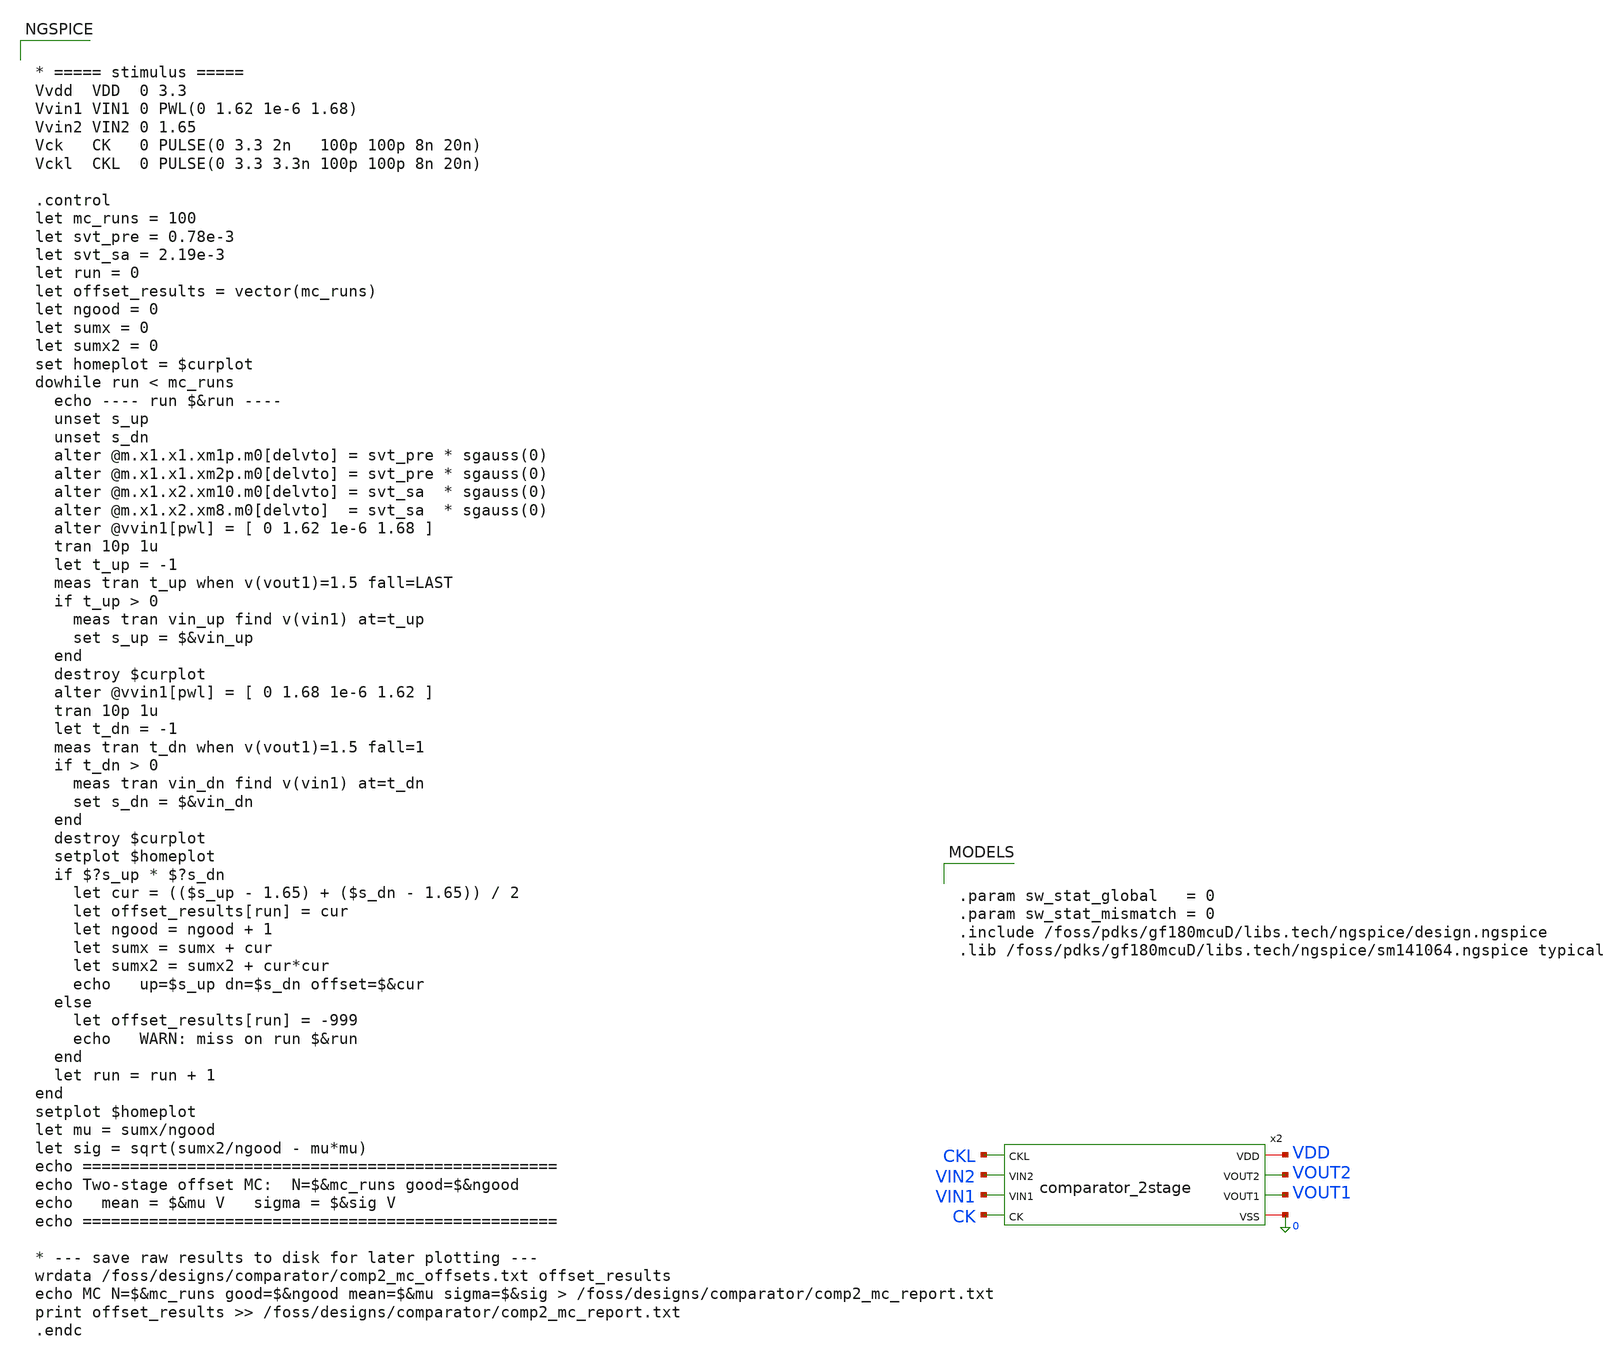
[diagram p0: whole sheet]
** sch_path: comparator_alt/schematic/tb_2stage.sch
**.subckt tb_2stage
x2 CKL VIN2 VDD VOUT2 VIN1 VOUT1 CK 0 comparator_2stage
**** begin user architecture code


.param sw_stat_global   = 0
.param sw_stat_mismatch = 0
.include /foss/pdks/gf180mcuD/libs.tech/ngspice/design.ngspice
.lib /foss/pdks/gf180mcuD/libs.tech/ngspice/sm141064.ngspice typical




* ===== stimulus =====
Vvdd  VDD  0 3.3
Vvin1 VIN1 0 PWL(0 1.62 1e-6 1.68)
Vvin2 VIN2 0 1.65
Vck   CK   0 PULSE(0 3.3 2n   100p 100p 8n 20n)
Vckl  CKL  0 PULSE(0 3.3 3.3n 100p 100p 8n 20n)

.control
let mc_runs = 100
let svt_pre = 0.78e-3
let svt_sa = 2.19e-3
let run = 0
let offset_results = vector(mc_runs)
let ngood = 0
let sumx = 0
let sumx2 = 0
set homeplot = $curplot
dowhile run < mc_runs
  echo ---- run $&run ----
  unset s_up
  unset s_dn
  alter @m.x1.x1.xm1p.m0[delvto] = svt_pre * sgauss(0)
  alter @m.x1.x1.xm2p.m0[delvto] = svt_pre * sgauss(0)
  alter @m.x1.x2.xm10.m0[delvto] = svt_sa  * sgauss(0)
  alter @m.x1.x2.xm8.m0[delvto]  = svt_sa  * sgauss(0)
  alter @vvin1[pwl] = [ 0 1.62 1e-6 1.68 ]
  tran 10p 1u
  let t_up = -1
  meas tran t_up when v(vout1)=1.5 fall=LAST
  if t_up > 0
    meas tran vin_up find v(vin1) at=t_up
    set s_up = $&vin_up
  end
  destroy $curplot
  alter @vvin1[pwl] = [ 0 1.68 1e-6 1.62 ]
  tran 10p 1u
  let t_dn = -1
  meas tran t_dn when v(vout1)=1.5 fall=1
  if t_dn > 0
    meas tran vin_dn find v(vin1) at=t_dn
    set s_dn = $&vin_dn
  end
  destroy $curplot
  setplot $homeplot
  if $?s_up * $?s_dn
    let cur = (($s_up - 1.65) + ($s_dn - 1.65)) / 2
    let offset_results[run] = cur
    let ngood = ngood + 1
    let sumx = sumx + cur
    let sumx2 = sumx2 + cur*cur
    echo   up=$s_up dn=$s_dn offset=$&cur
  else
    let offset_results[run] = -999
    echo   WARN: miss on run $&run
  end
  let run = run + 1
end
setplot $homeplot
let mu = sumx/ngood
let sig = sqrt(sumx2/ngood - mu*mu)
echo ==================================================
echo Two-stage offset MC:  N=$&mc_runs good=$&ngood
echo   mean = $&mu V   sigma = $&sig V
echo ==================================================

* --- save raw results to disk for later plotting ---
wrdata /foss/designs/comparator/comp2_mc_offsets.txt offset_results
echo MC N=$&mc_runs good=$&ngood mean=$&mu sigma=$&sig >
+ /foss/designs/comparator/comp2_mc_report.txt
print offset_results >> /foss/designs/comparator/comp2_mc_report.txt
.endc


**** end user architecture code
**.ends

* expanding   symbol:  comparator_alt/schematic/comparator_2stage.sym # of pins=8
** sym_path: comparator/schematic/comparator_2stage.sym
** sch_path: comparator/schematic/comparator_2stage.sch
.subckt comparator_2stage CKL VIN2 VDD VOUT2 VIN1 VOUT1 CK VSS
*.ipin CK
*.iopin VDD
*.iopin VSS
*.ipin VIN1
*.ipin VIN2
*.opin VOUT2
*.opin VOUT1
*.ipin CKL
x2 VDD DIP1 DIP2 VIN2 VIN1 CK VSS preamp_dyn
x4 VDD CKL VOUT2 VOUT1 DIP2 DIP1 VSS strongarm_2
.ends


* expanding   symbol:  comparator/schematic/preamp_dyn.sym # of pins=7
** sym_path: comparator_alt/schematic/preamp_dyn.sym
** sch_path: comparator_alt/schematic/preamp_dyn.sch
.subckt preamp_dyn VDD DIP2 DIP1 VIN2 VIN1 CK VSS
*.ipin VIN1
*.ipin VIN2
*.iopin VDD
*.iopin VSS
*.opin DIP1
*.opin DIP2
*.ipin CK
XM1P DIP1 VIN1 TAIL VSS nfet_03v3 L=1u W=4u nf=1 ad='int((nf+1)/2) * W/nf * 0.18u' as='int((nf+2)/2) * W/nf * 0.18u'
+ pd='2*int((nf+1)/2) * (W/nf + 0.18u)' ps='2*int((nf+2)/2) * (W/nf + 0.18u)' nrd='0.18u / W' nrs='0.18u / W'
+ sa=0 sb=0 sd=0 m=16
XMT1 TAIL CK VSS VSS nfet_03v3 L=1u W=1u nf=1 ad='int((nf+1)/2) * W/nf * 0.18u' as='int((nf+2)/2) * W/nf * 0.18u'
+ pd='2*int((nf+1)/2) * (W/nf + 0.18u)' ps='2*int((nf+2)/2) * (W/nf + 0.18u)' nrd='0.18u / W' nrs='0.18u / W'
+ sa=0 sb=0 sd=0 m=1
XM2P DIP2 VIN2 TAIL VSS nfet_03v3 L=1u W=4u nf=1 ad='int((nf+1)/2) * W/nf * 0.18u' as='int((nf+2)/2) * W/nf * 0.18u'
+ pd='2*int((nf+1)/2) * (W/nf + 0.18u)' ps='2*int((nf+2)/2) * (W/nf + 0.18u)' nrd='0.18u / W' nrs='0.18u / W'
+ sa=0 sb=0 sd=0 m=16
XMP1 DIP1 CK VDD VDD pfet_03v3 L=0.3u W=3u nf=1 ad='int((nf+1)/2) * W/nf * 0.18u' as='int((nf+2)/2) * W/nf * 0.18u'
+ pd='2*int((nf+1)/2) * (W/nf + 0.18u)' ps='2*int((nf+2)/2) * (W/nf + 0.18u)' nrd='0.18u / W' nrs='0.18u / W'
+ sa=0 sb=0 sd=0 m=1
XMP2 DIP2 CK VDD VDD pfet_03v3 L=0.3u W=3u nf=1 ad='int((nf+1)/2) * W/nf * 0.18u' as='int((nf+2)/2) * W/nf * 0.18u'
+ pd='2*int((nf+1)/2) * (W/nf + 0.18u)' ps='2*int((nf+2)/2) * (W/nf + 0.18u)' nrd='0.18u / W' nrs='0.18u / W'
+ sa=0 sb=0 sd=0 m=1
.ends


* expanding   symbol:  comparator/schematic/strongarm_2.sym # of pins=7
** sym_path: comparator_alt/schematic/strongarm_2.sym
** sch_path: comparator_alt/schematic/strongarm_2.sch
.subckt strongarm_2 VDD CK VOUT2 VOUT1 VIN1 VIN2 VSS
*.opin VOUT1
*.opin VOUT2
*.ipin VIN1
*.ipin VIN2
*.ipin CK
*.iopin VDD
*.iopin VSS
XM1 VOUT2 VOUT1 net1 VSS nfet_03v3 L=0.28u W=2u nf=1 ad='int((nf+1)/2) * W/nf * 0.18u' as='int((nf+2)/2) * W/nf * 0.18u'
+ pd='2*int((nf+1)/2) * (W/nf + 0.18u)' ps='2*int((nf+2)/2) * (W/nf + 0.18u)' nrd='0.18u / W' nrs='0.18u / W'
+ sa=0 sb=0 sd=0 m=1
XM2 VOUT1 VOUT2 VDD VDD pfet_03v3 L=0.28u W=0.42u nf=1 ad='int((nf+1)/2) * W/nf * 0.18u' as='int((nf+2)/2) * W/nf * 0.18u'
+ pd='2*int((nf+1)/2) * (W/nf + 0.18u)' ps='2*int((nf+2)/2) * (W/nf + 0.18u)' nrd='0.18u / W' nrs='0.18u / W'
+ sa=0 sb=0 sd=0 m=1
XM3 VOUT1 CK VDD VDD pfet_03v3 L=0.28u W=5u nf=1 ad='int((nf+1)/2) * W/nf * 0.18u' as='int((nf+2)/2) * W/nf * 0.18u'
+ pd='2*int((nf+1)/2) * (W/nf + 0.18u)' ps='2*int((nf+2)/2) * (W/nf + 0.18u)' nrd='0.18u / W' nrs='0.18u / W'
+ sa=0 sb=0 sd=0 m=1
XM4 net3 CK VDD VDD pfet_03v3 L=0.28u W=5u nf=1 ad='int((nf+1)/2) * W/nf * 0.18u' as='int((nf+2)/2) * W/nf * 0.18u'
+ pd='2*int((nf+1)/2) * (W/nf + 0.18u)' ps='2*int((nf+2)/2) * (W/nf + 0.18u)' nrd='0.18u / W' nrs='0.18u / W'
+ sa=0 sb=0 sd=0 m=1
XM5 net1 CK VDD VDD pfet_03v3 L=0.28u W=5u nf=1 ad='int((nf+1)/2) * W/nf * 0.18u' as='int((nf+2)/2) * W/nf * 0.18u'
+ pd='2*int((nf+1)/2) * (W/nf + 0.18u)' ps='2*int((nf+2)/2) * (W/nf + 0.18u)' nrd='0.18u / W' nrs='0.18u / W'
+ sa=0 sb=0 sd=0 m=1
XM6 VOUT2 CK VDD VDD pfet_03v3 L=0.28u W=5u nf=1 ad='int((nf+1)/2) * W/nf * 0.18u' as='int((nf+2)/2) * W/nf * 0.18u'
+ pd='2*int((nf+1)/2) * (W/nf + 0.18u)' ps='2*int((nf+2)/2) * (W/nf + 0.18u)' nrd='0.18u / W' nrs='0.18u / W'
+ sa=0 sb=0 sd=0 m=1
XM7 VOUT2 VOUT1 VDD VDD pfet_03v3 L=0.28u W=0.42u nf=1 ad='int((nf+1)/2) * W/nf * 0.18u' as='int((nf+2)/2) * W/nf * 0.18u'
+ pd='2*int((nf+1)/2) * (W/nf + 0.18u)' ps='2*int((nf+2)/2) * (W/nf + 0.18u)' nrd='0.18u / W' nrs='0.18u / W'
+ sa=0 sb=0 sd=0 m=1
XM8 net1 VIN2 net2 VSS nfet_03v3 L=1u W=8u nf=1 ad='int((nf+1)/2) * W/nf * 0.18u' as='int((nf+2)/2) * W/nf * 0.18u'
+ pd='2*int((nf+1)/2) * (W/nf + 0.18u)' ps='2*int((nf+2)/2) * (W/nf + 0.18u)' nrd='0.18u / W' nrs='0.18u / W'
+ sa=0 sb=0 sd=0 m=1
XM9 VOUT1 VOUT2 net3 VSS nfet_03v3 L=0.28u W=2u nf=1 ad='int((nf+1)/2) * W/nf * 0.18u' as='int((nf+2)/2) * W/nf * 0.18u'
+ pd='2*int((nf+1)/2) * (W/nf + 0.18u)' ps='2*int((nf+2)/2) * (W/nf + 0.18u)' nrd='0.18u / W' nrs='0.18u / W'
+ sa=0 sb=0 sd=0 m=1
XM10 net3 VIN1 net2 VSS nfet_03v3 L=1u W=8u nf=1 ad='int((nf+1)/2) * W/nf * 0.18u' as='int((nf+2)/2) * W/nf * 0.18u'
+ pd='2*int((nf+1)/2) * (W/nf + 0.18u)' ps='2*int((nf+2)/2) * (W/nf + 0.18u)' nrd='0.18u / W' nrs='0.18u / W'
+ sa=0 sb=0 sd=0 m=1
XM11 net2 CK VSS VSS nfet_03v3 L=0.28u W=2u nf=1 ad='int((nf+1)/2) * W/nf * 0.18u' as='int((nf+2)/2) * W/nf * 0.18u'
+ pd='2*int((nf+1)/2) * (W/nf + 0.18u)' ps='2*int((nf+2)/2) * (W/nf + 0.18u)' nrd='0.18u / W' nrs='0.18u / W'
+ sa=0 sb=0 sd=0 m=1
.ends

.end
